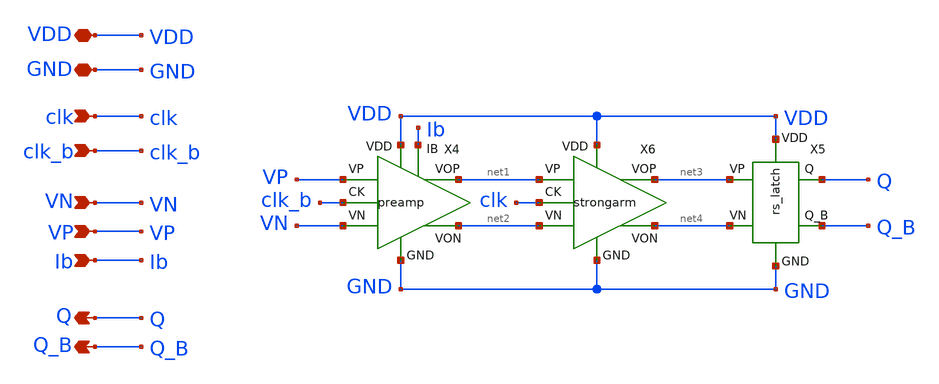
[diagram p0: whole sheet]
** sch_path: xschem/comparator/comparator.sch
**.subckt comparator VP VN VDD clk GND Q Q_B Ib clk_b
*.ipin VP
*.ipin VN
*.iopin VDD
*.ipin clk
*.iopin GND
*.opin Q
*.opin Q_B
*.ipin Ib
*.ipin clk_b
X4 VP VN GND net2 net1 VDD clk_b Ib preamp
X5 net3 net4 GND VDD Q Q_B rs_latch
X6 net1 net2 GND net4 net3 VDD clk strongarm
**.ends
.end
